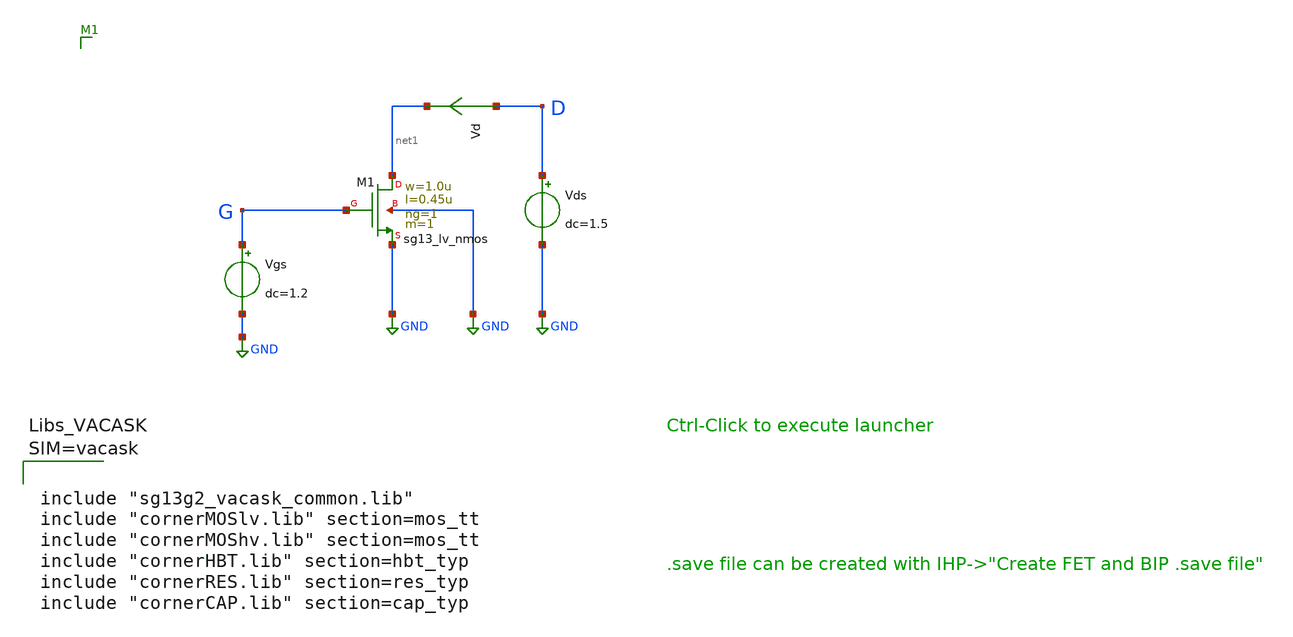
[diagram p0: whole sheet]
** sch_path: demo/ihp-sg13g2/dc_lv_nmos.sch
* Copyright 2023 IHP PDK Authors
**.subckt dc_lv_nmos
Vgs G GND dc=1.2
Vds D GND dc=1.5
Vd D net1 0
.save i(vd)
XM1 net1 G GND GND sg13_lv_nmos w=1.0u l=0.45u ng=1 m=1 mm_ok=1
**** begin user architecture code






**** end user architecture code
**.ends
.GLOBAL GND
.end
